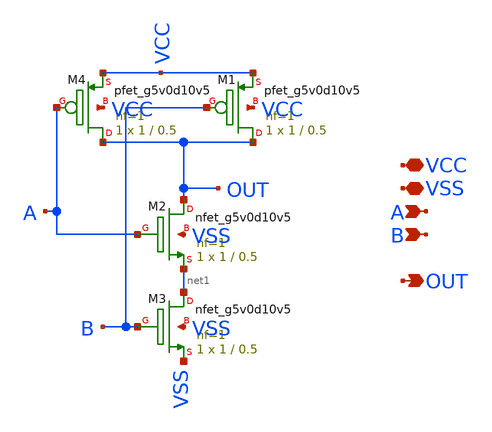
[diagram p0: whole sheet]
** sch_path: Comparator/schematic/Edge_pursuit_comparator/nand.sch
**.subckt nand VCC OUT B VSS A
*.iopin VCC
*.opin OUT
*.ipin B
*.iopin VSS
*.ipin A
XM1 OUT B VCC VCC sky130_fd_pr__pfet_g5v0d10v5 L=0.5 W=1 nf=1 ad='int((nf+1)/2) * W/nf * 0.29' as='int((nf+2)/2) * W/nf * 0.29'
+ pd='2*int((nf+1)/2) * (W/nf + 0.29)' ps='2*int((nf+2)/2) * (W/nf + 0.29)' nrd='0.29 / W' nrs='0.29 / W'
+ sa=0 sb=0 sd=0 mult=1 m=1
XM2 OUT A net1 VSS sky130_fd_pr__nfet_g5v0d10v5 L=0.5 W=1 nf=1 ad='int((nf+1)/2) * W/nf * 0.29' as='int((nf+2)/2) * W/nf * 0.29'
+ pd='2*int((nf+1)/2) * (W/nf + 0.29)' ps='2*int((nf+2)/2) * (W/nf + 0.29)' nrd='0.29 / W' nrs='0.29 / W'
+ sa=0 sb=0 sd=0 mult=1 m=1
XM3 net1 B VSS VSS sky130_fd_pr__nfet_g5v0d10v5 L=0.5 W=1 nf=1 ad='int((nf+1)/2) * W/nf * 0.29' as='int((nf+2)/2) * W/nf * 0.29'
+ pd='2*int((nf+1)/2) * (W/nf + 0.29)' ps='2*int((nf+2)/2) * (W/nf + 0.29)' nrd='0.29 / W' nrs='0.29 / W'
+ sa=0 sb=0 sd=0 mult=1 m=1
XM4 OUT A VCC VCC sky130_fd_pr__pfet_g5v0d10v5 L=0.5 W=1 nf=1 ad='int((nf+1)/2) * W/nf * 0.29' as='int((nf+2)/2) * W/nf * 0.29'
+ pd='2*int((nf+1)/2) * (W/nf + 0.29)' ps='2*int((nf+2)/2) * (W/nf + 0.29)' nrd='0.29 / W' nrs='0.29 / W'
+ sa=0 sb=0 sd=0 mult=1 m=1
**.ends
.end
